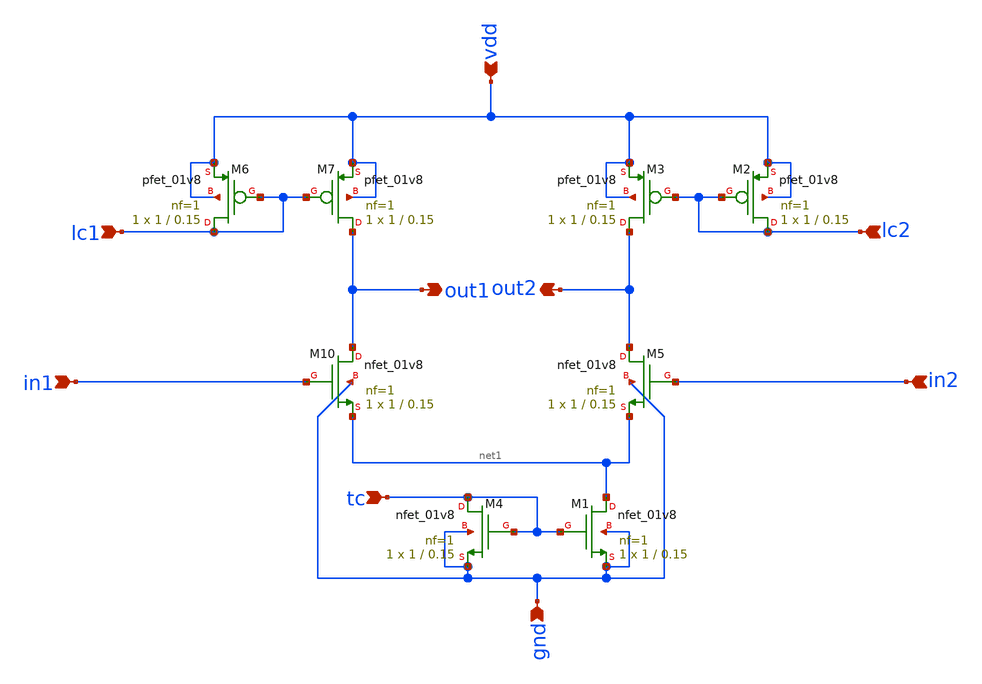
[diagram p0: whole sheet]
** sch_path: xschem/csfd-abstract.sch
**.subckt csfd-abstract vdd in1 in2 gnd out1 out2 tc lc1 lc2
*.ipin vdd
*.ipin in1
*.ipin in2
*.ipin gnd
*.opin out1
*.opin out2
*.ipin tc
*.ipin lc1
*.ipin lc2
XM10 out1 in1 net1 gnd sky130_fd_pr__nfet_01v8 L=0.15 W=1 nf=1 ad='int((nf+1)/2) * W/nf * 0.29' as='int((nf+2)/2) * W/nf * 0.29'
+ pd='2*int((nf+1)/2) * (W/nf + 0.29)' ps='2*int((nf+2)/2) * (W/nf + 0.29)' nrd='0.29 / W' nrs='0.29 / W'
+ sa=0 sb=0 sd=0 mult=1 m=1
XM3 out2 lc2 vdd vdd sky130_fd_pr__pfet_01v8 L=0.15 W=1 nf=1 ad='int((nf+1)/2) * W/nf * 0.29' as='int((nf+2)/2) * W/nf * 0.29'
+ pd='2*int((nf+1)/2) * (W/nf + 0.29)' ps='2*int((nf+2)/2) * (W/nf + 0.29)' nrd='0.29 / W' nrs='0.29 / W'
+ sa=0 sb=0 sd=0 mult=1 m=1
XM2 lc2 lc2 vdd vdd sky130_fd_pr__pfet_01v8 L=0.15 W=1 nf=1 ad='int((nf+1)/2) * W/nf * 0.29' as='int((nf+2)/2) * W/nf * 0.29'
+ pd='2*int((nf+1)/2) * (W/nf + 0.29)' ps='2*int((nf+2)/2) * (W/nf + 0.29)' nrd='0.29 / W' nrs='0.29 / W'
+ sa=0 sb=0 sd=0 mult=1 m=1
XM6 lc1 lc1 vdd vdd sky130_fd_pr__pfet_01v8 L=0.15 W=1 nf=1 ad='int((nf+1)/2) * W/nf * 0.29' as='int((nf+2)/2) * W/nf * 0.29'
+ pd='2*int((nf+1)/2) * (W/nf + 0.29)' ps='2*int((nf+2)/2) * (W/nf + 0.29)' nrd='0.29 / W' nrs='0.29 / W'
+ sa=0 sb=0 sd=0 mult=1 m=1
XM7 out1 lc1 vdd vdd sky130_fd_pr__pfet_01v8 L=0.15 W=1 nf=1 ad='int((nf+1)/2) * W/nf * 0.29' as='int((nf+2)/2) * W/nf * 0.29'
+ pd='2*int((nf+1)/2) * (W/nf + 0.29)' ps='2*int((nf+2)/2) * (W/nf + 0.29)' nrd='0.29 / W' nrs='0.29 / W'
+ sa=0 sb=0 sd=0 mult=1 m=1
XM5 out2 in2 net1 gnd sky130_fd_pr__nfet_01v8 L=0.15 W=1 nf=1 ad='int((nf+1)/2) * W/nf * 0.29' as='int((nf+2)/2) * W/nf * 0.29'
+ pd='2*int((nf+1)/2) * (W/nf + 0.29)' ps='2*int((nf+2)/2) * (W/nf + 0.29)' nrd='0.29 / W' nrs='0.29 / W'
+ sa=0 sb=0 sd=0 mult=1 m=1
XM1 net1 tc gnd gnd sky130_fd_pr__nfet_01v8 L=0.15 W=1 nf=1 ad='int((nf+1)/2) * W/nf * 0.29' as='int((nf+2)/2) * W/nf * 0.29'
+ pd='2*int((nf+1)/2) * (W/nf + 0.29)' ps='2*int((nf+2)/2) * (W/nf + 0.29)' nrd='0.29 / W' nrs='0.29 / W'
+ sa=0 sb=0 sd=0 mult=1 m=1
XM4 tc tc gnd gnd sky130_fd_pr__nfet_01v8 L=0.15 W=1 nf=1 ad='int((nf+1)/2) * W/nf * 0.29' as='int((nf+2)/2) * W/nf * 0.29'
+ pd='2*int((nf+1)/2) * (W/nf + 0.29)' ps='2*int((nf+2)/2) * (W/nf + 0.29)' nrd='0.29 / W' nrs='0.29 / W'
+ sa=0 sb=0 sd=0 mult=1 m=1
**** begin user architecture code
 ** manual skywater pdks install (with patches applied)
* .lib $::SKYWATER_MODELS/models/sky130.lib.spice tt

** opencircuitdesign pdks install
.lib $::SKYWATER_MODELS/sky130.lib.spice tt

.param mc_mm_switch=0
.param mc_pr_switch=0



.tran 0.000001s 0.00001s
.plot v(drain1) v(drain2)


**** end user architecture code
**.ends
.end
